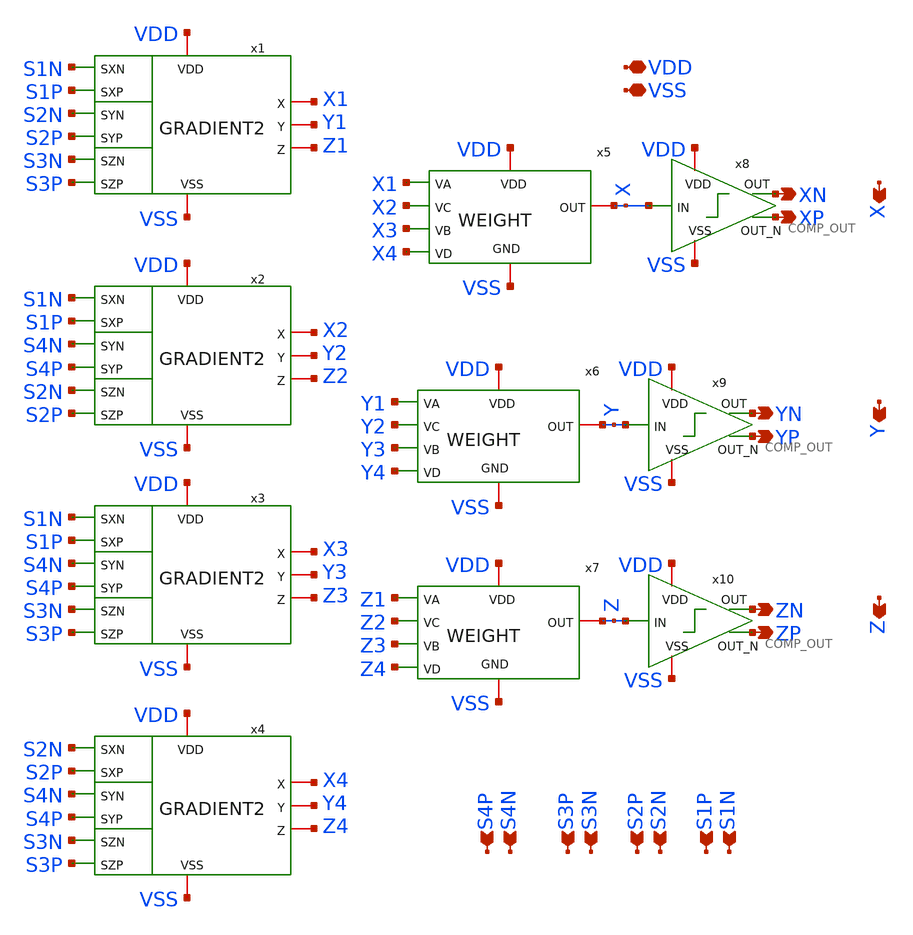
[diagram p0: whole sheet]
** sch_path: FINAL/XSCHEM_v3/GRADIENT_NAV2_V3.sch
**.subckt GRADIENT_NAV2_V3 S1N VDD XP VSS S1P S2N S2P S3N S3P S4N S4P XN YP YN ZP ZN X Y Z
*.ipin S1N
*.iopin VDD
*.opin XP
*.iopin VSS
*.ipin S1P
*.ipin S2N
*.ipin S2P
*.ipin S3N
*.ipin S3P
*.ipin S4N
*.ipin S4P
*.opin XN
*.opin YP
*.opin YN
*.opin ZP
*.opin ZN
*.opin X
*.opin Y
*.opin Z
x5 VDD VSS X X1 X2 X3 X4 WEIGHT
x6 VDD VSS Y Y1 Y2 Y3 Y4 WEIGHT
x7 VDD VSS Z Z1 Z2 Z3 Z4 WEIGHT
x8 VDD XN X XP VSS COMP_OUT
x9 VDD YN Y YP VSS COMP_OUT
x10 VDD ZN Z ZP VSS COMP_OUT
x1 S1N S1P VDD X1 S2N Y1 Z1 S2P VSS S3N S3P GRADIENT2
x2 S1N S1P VDD X2 S4N Y2 Z2 S4P VSS S2N S2P GRADIENT2
x3 S1N S1P VDD X3 S4N Y3 Z3 S4P VSS S3N S3P GRADIENT2
x4 S2N S2P VDD X4 S4N Y4 Z4 S4P VSS S3N S3P GRADIENT2
**** begin user architecture code


* Decoupling capacitors: NMOS and PMOS in inversion dropped into
* the gaps between macros. WRITTEN BY scripts/decap_fill.py -- do
* not edit by hand: it must be exactly what is in the GDS.
XMdecn0 VSS VDD VSS VSS nfet_06v0 L=2.0u W=1.0u nf=1 m=1
XMdecn1 VSS VDD VSS VSS nfet_06v0 L=2.0u W=1.0u nf=1 m=1
XMdecn2 VSS VDD VSS VSS nfet_06v0 L=2.0u W=1.0u nf=1 m=1
XMdecn3 VSS VDD VSS VSS nfet_06v0 L=2.0u W=1.0u nf=1 m=1
XMdecn4 VSS VDD VSS VSS nfet_06v0 L=2.0u W=1.0u nf=1 m=1
XMdecn5 VSS VDD VSS VSS nfet_06v0 L=2.0u W=1.0u nf=1 m=1
XMdecn6 VSS VDD VSS VSS nfet_06v0 L=2.0u W=1.0u nf=1 m=1
XMdecn7 VSS VDD VSS VSS nfet_06v0 L=2.0u W=1.0u nf=1 m=1
XMdecn8 VSS VDD VSS VSS nfet_06v0 L=2.0u W=1.0u nf=1 m=1
XMdecn9 VSS VDD VSS VSS nfet_06v0 L=2.0u W=1.0u nf=1 m=1
XMdecn10 VSS VDD VSS VSS nfet_06v0 L=2.0u W=1.0u nf=1 m=1
XMdecn11 VSS VDD VSS VSS nfet_06v0 L=2.0u W=1.0u nf=1 m=1
XMdecn12 VSS VDD VSS VSS nfet_06v0 L=2.0u W=1.0u nf=1 m=1
XMdecp13 VDD VSS VDD VDD pfet_06v0 L=2.0u W=1.0u nf=1 m=1
XMdecp14 VDD VSS VDD VDD pfet_06v0 L=2.0u W=1.0u nf=1 m=1
XMdecp15 VDD VSS VDD VDD pfet_06v0 L=2.0u W=1.0u nf=1 m=1
XMdecp16 VDD VSS VDD VDD pfet_06v0 L=2.0u W=1.0u nf=1 m=1
XMdecp17 VDD VSS VDD VDD pfet_06v0 L=2.0u W=1.0u nf=1 m=1
XMdecp18 VDD VSS VDD VDD pfet_06v0 L=2.0u W=1.0u nf=1 m=1
XMdecp19 VDD VSS VDD VDD pfet_06v0 L=2.0u W=1.0u nf=1 m=1
XMdecp20 VDD VSS VDD VDD pfet_06v0 L=2.0u W=1.0u nf=1 m=1
XMdecp21 VDD VSS VDD VDD pfet_06v0 L=2.0u W=1.0u nf=1 m=1
XMdecp22 VDD VSS VDD VDD pfet_06v0 L=2.0u W=1.0u nf=1 m=1
XMdecp23 VDD VSS VDD VDD pfet_06v0 L=2.0u W=1.0u nf=1 m=1
XMdecp24 VDD VSS VDD VDD pfet_06v0 L=2.0u W=1.0u nf=1 m=1
XMdecn25 VSS VDD VSS VSS nfet_06v0 L=2.0u W=18.0u nf=1 m=1
XMdecn26 VSS VDD VSS VSS nfet_06v0 L=2.0u W=18.0u nf=1 m=1
XMdecn27 VSS VDD VSS VSS nfet_06v0 L=2.0u W=18.0u nf=1 m=1
XMdecp28 VDD VSS VDD VDD pfet_06v0 L=2.0u W=18.0u nf=1 m=1
XMdecp29 VDD VSS VDD VDD pfet_06v0 L=2.0u W=18.0u nf=1 m=1
XMdecn30 VSS VDD VSS VSS nfet_06v0 L=2.0u W=18.0u nf=1 m=1
XMdecn31 VSS VDD VSS VSS nfet_06v0 L=2.0u W=18.0u nf=1 m=1
XMdecn32 VSS VDD VSS VSS nfet_06v0 L=2.0u W=18.0u nf=1 m=1
XMdecp33 VDD VSS VDD VDD pfet_06v0 L=2.0u W=18.0u nf=1 m=1
XMdecp34 VDD VSS VDD VDD pfet_06v0 L=2.0u W=18.0u nf=1 m=1
XMdecn35 VSS VDD VSS VSS nfet_06v0 L=2.0u W=18.0u nf=1 m=1
XMdecn36 VSS VDD VSS VSS nfet_06v0 L=2.0u W=18.0u nf=1 m=1
XMdecn37 VSS VDD VSS VSS nfet_06v0 L=2.0u W=18.0u nf=1 m=1
XMdecp38 VDD VSS VDD VDD pfet_06v0 L=2.0u W=18.0u nf=1 m=1
XMdecp39 VDD VSS VDD VDD pfet_06v0 L=2.0u W=18.0u nf=1 m=1
XMdecn40 VSS VDD VSS VSS nfet_06v0 L=2.0u W=18.0u nf=1 m=1
XMdecn41 VSS VDD VSS VSS nfet_06v0 L=2.0u W=18.0u nf=1 m=1
XMdecp42 VDD VSS VDD VDD pfet_06v0 L=2.0u W=18.0u nf=1 m=1
XMdecp43 VDD VSS VDD VDD pfet_06v0 L=2.0u W=18.0u nf=1 m=1
XMdecn44 VSS VDD VSS VSS nfet_06v0 L=2.0u W=18.0u nf=1 m=1
XMdecn45 VSS VDD VSS VSS nfet_06v0 L=2.0u W=18.0u nf=1 m=1
XMdecp46 VDD VSS VDD VDD pfet_06v0 L=2.0u W=18.0u nf=1 m=1
XMdecp47 VDD VSS VDD VDD pfet_06v0 L=2.0u W=18.0u nf=1 m=1
XMdecn48 VSS VDD VSS VSS nfet_06v0 L=2.0u W=18.0u nf=1 m=1
XMdecn49 VSS VDD VSS VSS nfet_06v0 L=2.0u W=18.0u nf=1 m=1
XMdecp50 VDD VSS VDD VDD pfet_06v0 L=2.0u W=18.0u nf=1 m=1
XMdecp51 VDD VSS VDD VDD pfet_06v0 L=2.0u W=18.0u nf=1 m=1
XMdecn52 VSS VDD VSS VSS nfet_06v0 L=2.0u W=18.0u nf=1 m=1
XMdecn53 VSS VDD VSS VSS nfet_06v0 L=2.0u W=18.0u nf=1 m=1
XMdecp54 VDD VSS VDD VDD pfet_06v0 L=2.0u W=18.0u nf=1 m=1
XMdecp55 VDD VSS VDD VDD pfet_06v0 L=2.0u W=18.0u nf=1 m=1
XMdecn56 VSS VDD VSS VSS nfet_06v0 L=2.0u W=18.0u nf=1 m=1
XMdecn57 VSS VDD VSS VSS nfet_06v0 L=2.0u W=18.0u nf=1 m=1
XMdecp58 VDD VSS VDD VDD pfet_06v0 L=2.0u W=18.0u nf=1 m=1
XMdecp59 VDD VSS VDD VDD pfet_06v0 L=2.0u W=18.0u nf=1 m=1
XMdecn60 VSS VDD VSS VSS nfet_06v0 L=2.0u W=18.0u nf=1 m=1
XMdecn61 VSS VDD VSS VSS nfet_06v0 L=2.0u W=18.0u nf=1 m=1
XMdecp62 VDD VSS VDD VDD pfet_06v0 L=2.0u W=18.0u nf=1 m=1
XMdecp63 VDD VSS VDD VDD pfet_06v0 L=2.0u W=18.0u nf=1 m=1
XMdecn64 VSS VDD VSS VSS nfet_06v0 L=2.0u W=18.0u nf=1 m=1
XMdecn65 VSS VDD VSS VSS nfet_06v0 L=2.0u W=18.0u nf=1 m=1
XMdecp66 VDD VSS VDD VDD pfet_06v0 L=2.0u W=18.0u nf=1 m=1
XMdecp67 VDD VSS VDD VDD pfet_06v0 L=2.0u W=18.0u nf=1 m=1
XMdecn68 VSS VDD VSS VSS nfet_06v0 L=2.0u W=18.0u nf=1 m=1
XMdecn69 VSS VDD VSS VSS nfet_06v0 L=2.0u W=18.0u nf=1 m=1
XMdecp70 VDD VSS VDD VDD pfet_06v0 L=2.0u W=18.0u nf=1 m=1
XMdecp71 VDD VSS VDD VDD pfet_06v0 L=2.0u W=18.0u nf=1 m=1
XMdecn72 VSS VDD VSS VSS nfet_06v0 L=2.0u W=18.0u nf=1 m=1
XMdecn73 VSS VDD VSS VSS nfet_06v0 L=2.0u W=18.0u nf=1 m=1
XMdecp74 VDD VSS VDD VDD pfet_06v0 L=2.0u W=18.0u nf=1 m=1
XMdecp75 VDD VSS VDD VDD pfet_06v0 L=2.0u W=18.0u nf=1 m=1
XMdecn76 VSS VDD VSS VSS nfet_06v0 L=2.0u W=9.75u nf=1 m=1
XMdecn77 VSS VDD VSS VSS nfet_06v0 L=2.0u W=9.75u nf=1 m=1
XMdecp78 VDD VSS VDD VDD pfet_06v0 L=2.0u W=9.75u nf=1 m=1
XMdecp79 VDD VSS VDD VDD pfet_06v0 L=2.0u W=9.75u nf=1 m=1
XMdecn80 VSS VDD VSS VSS nfet_06v0 L=2.0u W=9.75u nf=1 m=1
XMdecn81 VSS VDD VSS VSS nfet_06v0 L=2.0u W=9.75u nf=1 m=1
XMdecp82 VDD VSS VDD VDD pfet_06v0 L=2.0u W=9.75u nf=1 m=1
XMdecp83 VDD VSS VDD VDD pfet_06v0 L=2.0u W=9.75u nf=1 m=1
XMdecn84 VSS VDD VSS VSS nfet_06v0 L=2.0u W=9.75u nf=1 m=1
XMdecn85 VSS VDD VSS VSS nfet_06v0 L=2.0u W=9.75u nf=1 m=1
XMdecp86 VDD VSS VDD VDD pfet_06v0 L=2.0u W=9.75u nf=1 m=1
XMdecp87 VDD VSS VDD VDD pfet_06v0 L=2.0u W=9.75u nf=1 m=1
XMdecn88 VSS VDD VSS VSS nfet_06v0 L=2.0u W=9.75u nf=1 m=1
XMdecn89 VSS VDD VSS VSS nfet_06v0 L=2.0u W=9.75u nf=1 m=1
XMdecp90 VDD VSS VDD VDD pfet_06v0 L=2.0u W=9.75u nf=1 m=1
XMdecp91 VDD VSS VDD VDD pfet_06v0 L=2.0u W=9.75u nf=1 m=1
XMdecn92 VSS VDD VSS VSS nfet_06v0 L=2.0u W=9.75u nf=1 m=1
XMdecn93 VSS VDD VSS VSS nfet_06v0 L=2.0u W=9.75u nf=1 m=1
XMdecp94 VDD VSS VDD VDD pfet_06v0 L=2.0u W=9.75u nf=1 m=1
XMdecp95 VDD VSS VDD VDD pfet_06v0 L=2.0u W=9.75u nf=1 m=1
XMdecn96 VSS VDD VSS VSS nfet_06v0 L=2.0u W=9.75u nf=1 m=1
XMdecn97 VSS VDD VSS VSS nfet_06v0 L=2.0u W=9.75u nf=1 m=1
XMdecp98 VDD VSS VDD VDD pfet_06v0 L=2.0u W=9.75u nf=1 m=1
XMdecp99 VDD VSS VDD VDD pfet_06v0 L=2.0u W=9.75u nf=1 m=1
XMdecn100 VSS VDD VSS VSS nfet_06v0 L=2.0u W=9.75u nf=1 m=1
XMdecn101 VSS VDD VSS VSS nfet_06v0 L=2.0u W=9.75u nf=1 m=1
XMdecp102 VDD VSS VDD VDD pfet_06v0 L=2.0u W=9.75u nf=1 m=1
XMdecp103 VDD VSS VDD VDD pfet_06v0 L=2.0u W=9.75u nf=1 m=1
XMdecn104 VSS VDD VSS VSS nfet_06v0 L=2.0u W=9.75u nf=1 m=1
XMdecn105 VSS VDD VSS VSS nfet_06v0 L=2.0u W=9.75u nf=1 m=1
XMdecp106 VDD VSS VDD VDD pfet_06v0 L=2.0u W=9.75u nf=1 m=1
XMdecp107 VDD VSS VDD VDD pfet_06v0 L=2.0u W=9.75u nf=1 m=1
XMdecn108 VSS VDD VSS VSS nfet_06v0 L=2.0u W=9.75u nf=1 m=1
XMdecn109 VSS VDD VSS VSS nfet_06v0 L=2.0u W=9.75u nf=1 m=1
XMdecp110 VDD VSS VDD VDD pfet_06v0 L=2.0u W=9.75u nf=1 m=1
XMdecp111 VDD VSS VDD VDD pfet_06v0 L=2.0u W=9.75u nf=1 m=1
XMdecn112 VSS VDD VSS VSS nfet_06v0 L=2.0u W=9.75u nf=1 m=1
XMdecn113 VSS VDD VSS VSS nfet_06v0 L=2.0u W=9.75u nf=1 m=1
XMdecp114 VDD VSS VDD VDD pfet_06v0 L=2.0u W=9.75u nf=1 m=1
XMdecp115 VDD VSS VDD VDD pfet_06v0 L=2.0u W=9.75u nf=1 m=1
XMdecn116 VSS VDD VSS VSS nfet_06v0 L=2.0u W=9.75u nf=1 m=1
XMdecn117 VSS VDD VSS VSS nfet_06v0 L=2.0u W=9.75u nf=1 m=1
XMdecp118 VDD VSS VDD VDD pfet_06v0 L=2.0u W=9.75u nf=1 m=1
XMdecp119 VDD VSS VDD VDD pfet_06v0 L=2.0u W=9.75u nf=1 m=1
XMdecn120 VSS VDD VSS VSS nfet_06v0 L=2.0u W=9.75u nf=1 m=1
XMdecn121 VSS VDD VSS VSS nfet_06v0 L=2.0u W=9.75u nf=1 m=1
XMdecp122 VDD VSS VDD VDD pfet_06v0 L=2.0u W=9.75u nf=1 m=1
XMdecp123 VDD VSS VDD VDD pfet_06v0 L=2.0u W=9.75u nf=1 m=1
XMdecn124 VSS VDD VSS VSS nfet_06v0 L=2.0u W=18.0u nf=1 m=1
XMdecp125 VDD VSS VDD VDD pfet_06v0 L=2.0u W=18.0u nf=1 m=1
XMdecn126 VSS VDD VSS VSS nfet_06v0 L=2.0u W=18.0u nf=1 m=1
XMdecp127 VDD VSS VDD VDD pfet_06v0 L=2.0u W=18.0u nf=1 m=1
XMdecn128 VSS VDD VSS VSS nfet_06v0 L=2.0u W=18.0u nf=1 m=1
XMdecp129 VDD VSS VDD VDD pfet_06v0 L=2.0u W=18.0u nf=1 m=1
XMdecn130 VSS VDD VSS VSS nfet_06v0 L=2.0u W=9.75u nf=1 m=1
XMdecp131 VDD VSS VDD VDD pfet_06v0 L=2.0u W=9.75u nf=1 m=1
XMdecn132 VSS VDD VSS VSS nfet_06v0 L=2.0u W=9.75u nf=1 m=1
XMdecp133 VDD VSS VDD VDD pfet_06v0 L=2.0u W=9.75u nf=1 m=1
XMdecn134 VSS VDD VSS VSS nfet_06v0 L=2.0u W=9.75u nf=1 m=1
XMdecp135 VDD VSS VDD VDD pfet_06v0 L=2.0u W=9.75u nf=1 m=1
XMdecn136 VSS VDD VSS VSS nfet_06v0 L=2.0u W=9.75u nf=1 m=1
XMdecp137 VDD VSS VDD VDD pfet_06v0 L=2.0u W=9.75u nf=1 m=1
XMdecn138 VSS VDD VSS VSS nfet_06v0 L=2.0u W=1.0u nf=1 m=1
XMdecn139 VSS VDD VSS VSS nfet_06v0 L=2.0u W=1.0u nf=1 m=1
XMdecp140 VDD VSS VDD VDD pfet_06v0 L=2.0u W=1.0u nf=1 m=1
XMdecp141 VDD VSS VDD VDD pfet_06v0 L=2.0u W=1.0u nf=1 m=1
XMdecn142 VSS VDD VSS VSS nfet_06v0 L=2.0u W=1.0u nf=1 m=1
XMdecn143 VSS VDD VSS VSS nfet_06v0 L=2.0u W=1.0u nf=1 m=1
XMdecp144 VDD VSS VDD VDD pfet_06v0 L=2.0u W=1.0u nf=1 m=1
XMdecp145 VDD VSS VDD VDD pfet_06v0 L=2.0u W=1.0u nf=1 m=1
XMdecn146 VSS VDD VSS VSS nfet_06v0 L=2.0u W=1.0u nf=1 m=1
XMdecn147 VSS VDD VSS VSS nfet_06v0 L=2.0u W=1.0u nf=1 m=1
XMdecp148 VDD VSS VDD VDD pfet_06v0 L=2.0u W=1.0u nf=1 m=1
XMdecp149 VDD VSS VDD VDD pfet_06v0 L=2.0u W=1.0u nf=1 m=1
XMdecn150 VSS VDD VSS VSS nfet_06v0 L=2.0u W=1.0u nf=1 m=1
XMdecp151 VDD VSS VDD VDD pfet_06v0 L=2.0u W=1.0u nf=1 m=1
XMdecn152 VSS VDD VSS VSS nfet_06v0 L=2.0u W=1.0u nf=1 m=1
XMdecp153 VDD VSS VDD VDD pfet_06v0 L=2.0u W=1.0u nf=1 m=1
XMdecn154 VSS VDD VSS VSS nfet_06v0 L=2.0u W=1.0u nf=1 m=1
XMdecp155 VDD VSS VDD VDD pfet_06v0 L=2.0u W=1.0u nf=1 m=1


**** end user architecture code
**.ends
.end
